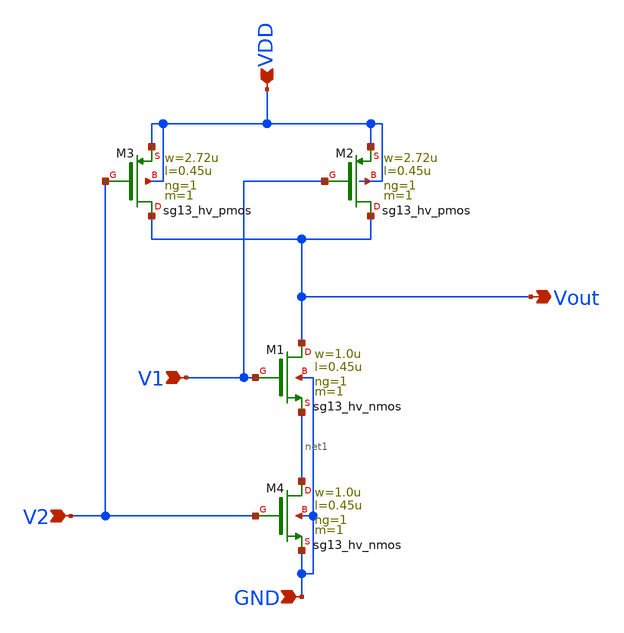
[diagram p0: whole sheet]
** sch_path: Taller2/Resuelto/Nand.sch
**.subckt Nand V1 V2 VDD GND Vout
*.ipin V1
*.ipin V2
*.ipin VDD
*.ipin GND
*.opin Vout
XM1 Vout V1 net1 GND sg13_hv_nmos w=1.0u l=0.45u ng=1 m=1 mm_ok=1
XM2 Vout V1 VDD VDD sg13_hv_pmos w=2.72u l=0.45u ng=1 m=1 mm_ok=1
XM3 Vout V2 VDD VDD sg13_hv_pmos w=2.72u l=0.45u ng=1 m=1 mm_ok=1
XM4 net1 V2 GND GND sg13_hv_nmos w=1.0u l=0.45u ng=1 m=1 mm_ok=1
**.ends
.end
